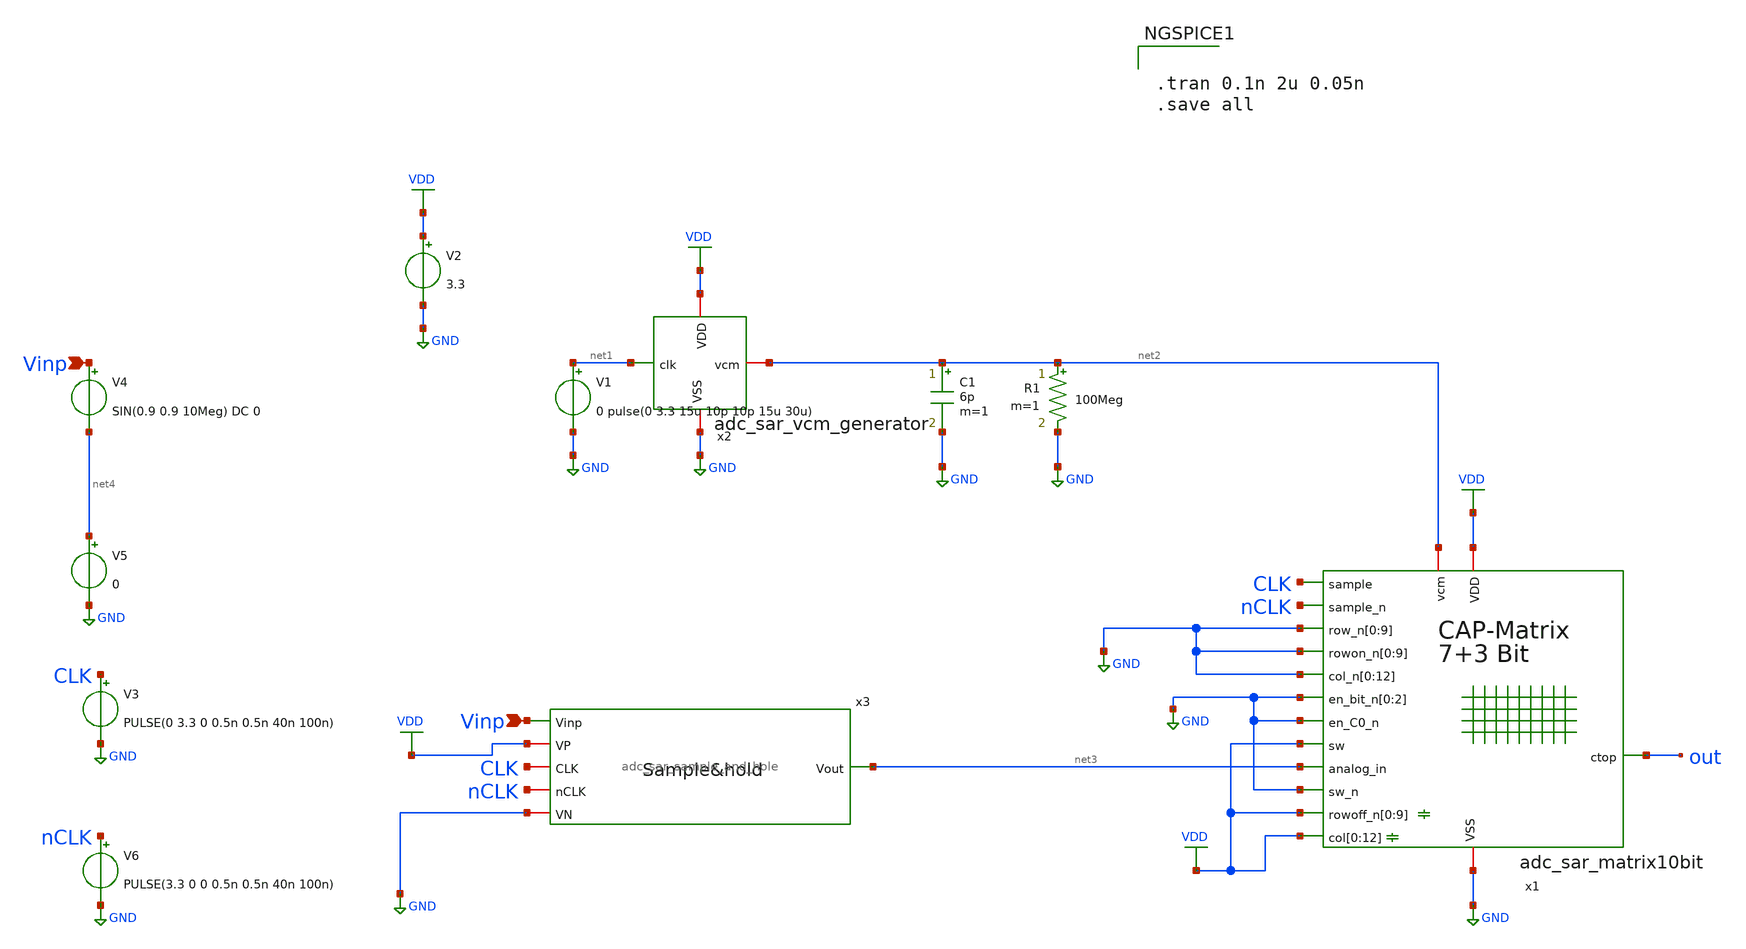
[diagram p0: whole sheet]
** sch_path: adc_sar_matrix10bit_tb.sch
**.subckt adc_sar_matrix10bit_tb Vinp Vinp
*.ipin Vinp
*.ipin Vinp
x1 GND GND GND GND GND GND GND GND GND GND GND GND GND GND GND GND GND GND GND GND VDD VDD VDD VDD
+ VDD VDD VDD VDD VDD VDD GND GND GND GND GND GND GND GND GND GND GND GND GND VDD VDD VDD VDD VDD VDD VDD
+ VDD VDD VDD VDD VDD VDD VDD GND net2 CLK nCLK GND GND GND GND VDD GND net3 out adc_sar_matrix10bit
x2 VDD net2 net1 GND adc_sar_vcm_generator
C1 net2 GND 6p m=1
R1 net2 GND 100Meg m=1
V1 net1 GND 0 pulse(0 3.3 15u 10p 10p 15u 30u)
V2 VDD GND 3.3
x3 VDD CLK net3 nCLK Vinp GND adc_sar_sample_and_hole
V4 Vinp net4 SIN(0.9 0.9 10Meg) DC 0
V5 net4 GND 0
V3 CLK GND PULSE(0 3.3 0 0.5n 0.5n 40n 100n)

V6 nCLK GND PULSE(3.3 0 0 0.5n 0.5n 40n 100n)

**** begin user architecture code


.tran 0.1n 2u 0.05n
.save all



.include /home/tien/conda-gf180mcu-env/envs/gf180mcu-env/share/pdk/gf180mcuC/libs.tech/ngspice/design.ngspice
.lib /home/tien/conda-gf180mcu-env/envs/gf180mcu-env/share/pdk/gf180mcuC/libs.tech/ngspice/smbb000149.ngspice typical
.lib /home/tien/conda-gf180mcu-env/envs/gf180mcu-env/share/pdk/gf180mcuC/libs.tech/ngspice/sm141064.ngspice cap_mim
.lib /home/tien/conda-gf180mcu-env/envs/gf180mcu-env/share/pdk/gf180mcuC/libs.tech/ngspice/sm141064.ngspice mimcap_typical
.lib /home/tien/conda-gf180mcu-env/envs/gf180mcu-env/share/pdk/gf180mcuC/libs.tech/ngspice/sm141064.ngspice res_typical
.lib /home/tien/conda-gf180mcu-env/envs/gf180mcu-env/share/pdk/gf180mcuC/libs.tech/ngspice/sm141064.ngspice moscap_typical
.lib /home/tien/conda-gf180mcu-env/envs/gf180mcu-env/share/pdk/gf180mcuC/libs.tech/ngspice/sm141064.ngspice diode_typical
.lib /home/tien/conda-gf180mcu-env/envs/gf180mcu-env/share/pdk/gf180mcuC/libs.tech/ngspice/sm141064.ngspice typical

**** end user architecture code
**.ends
.GLOBAL GND
.GLOBAL VDD
.end
